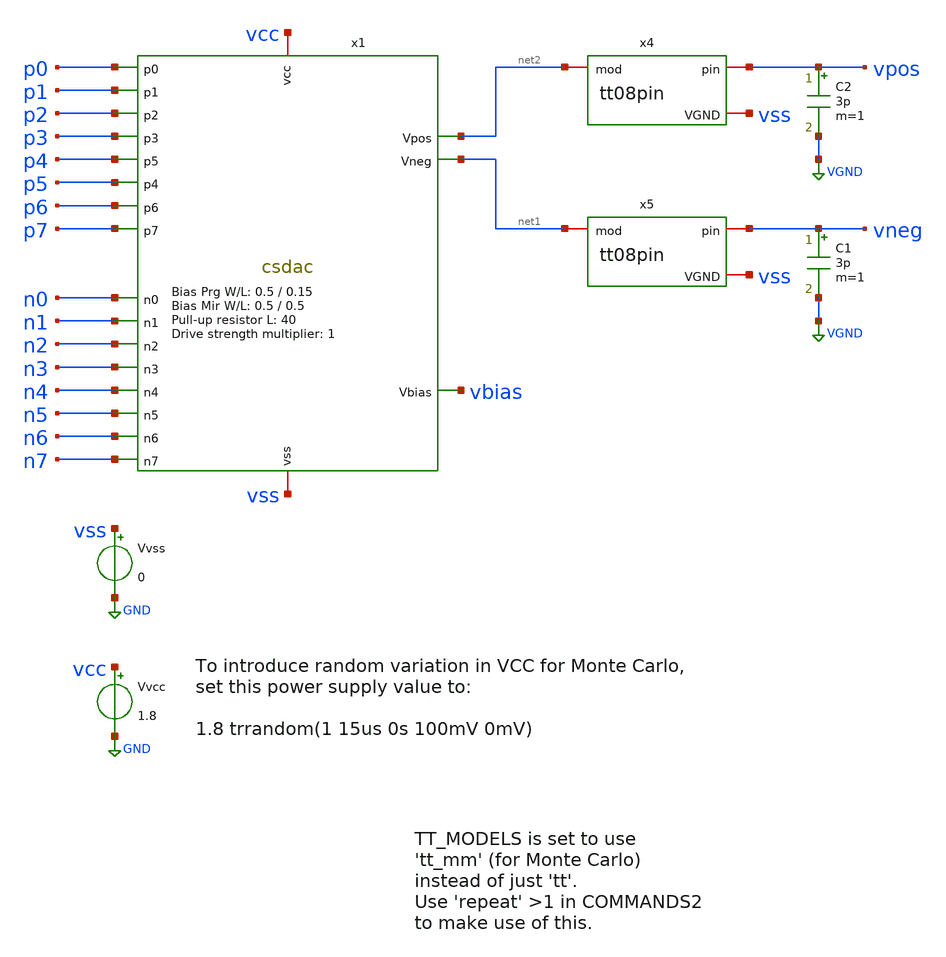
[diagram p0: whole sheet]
** sch_path: xschem/tb_csdac.sch
**.subckt tb_csdac
Vvcc vcc GND 1.8
Vvss vss GND 0
x1 vcc vss p0 p1 p2 p3 p4 p5 p6 p7 n0 n1 n2 n3 n4 n5 n6 n7 net2 net1 vbias csdac RPUL=40 MULTI=1
+ BIASPRG_W=0.5 BIASPRG_L=0.15 BIASMIR_W=0.5 BIASMIR_L=0.5
x4 vpos net2 vss tt08pin
x5 vneg net1 vss tt08pin
C2 vpos VGND 3p m=1
C1 vneg VGND 3p m=1
**** begin user architecture code



.param singlebits=0
.IF (singlebits == 1)
* Mode to just test each binary-weighted level:
Vxp0 p0 GND pulse 0v 1.8v 1u 1n 1n 1u 10u
Vxp1 p1 GND pulse 0v 1.8v 2u 1n 1n 1u 10u
Vxp2 p2 GND pulse 0v 1.8v 3u 1n 1n 1u 10u
Vxp3 p3 GND pulse 0v 1.8v 4u 1n 1n 1u 10u
Vxp4 p4 GND pulse 0v 1.8v 5u 1n 1n 1u 10u
Vxp5 p5 GND pulse 0v 1.8v 6u 1n 1n 1u 10u
Vxp6 p6 GND pulse 0v 1.8v 7u 1n 1n 1u 10u
Vxp7 p7 GND pulse 0v 1.8v 8u 1n 1n 1u 10u
Vxn0 n0 GND pulse 1.8v 0v 1u 1n 1n 1u 10u
Vxn1 n1 GND pulse 1.8v 0v 2u 1n 1n 1u 10u
Vxn2 n2 GND pulse 1.8v 0v 3u 1n 1n 1u 10u
Vxn3 n3 GND pulse 1.8v 0v 4u 1n 1n 1u 10u
Vxn4 n4 GND pulse 1.8v 0v 5u 1n 1n 1u 10u
Vxn5 n5 GND pulse 1.8v 0v 6u 1n 1n 1u 10u
Vxn6 n6 GND pulse 1.8v 0v 7u 1n 1n 1u 10u
Vxn7 n7 GND pulse 1.8v 0v 8u 1n 1n 1u 10u
.ELSEIF (singlebits == 0)
* Mode to test full 0..255 trange:
Vxp0 p0 GND pulse 1.8v 0v 0n 1n 1n 39n 80n
Vxp1 p1 GND pulse 1.8v 0v 0n 1n 1n 79n 160n
Vxp2 p2 GND pulse 1.8v 0v 0n 1n 1n 159n 320n
Vxp3 p3 GND pulse 1.8v 0v 0n 1n 1n 319n 640n
Vxp4 p4 GND pulse 1.8v 0v 0n 1n 1n 639n 1280n
Vxp5 p5 GND pulse 1.8v 0v 0n 1n 1n 1279n 2560n
Vxp6 p6 GND pulse 1.8v 0v 0n 1n 1n 2559n 5120n
Vxp7 p7 GND pulse 1.8v 0v 0n 1n 1n 5119n 10240n
Vxn0 n0 GND pulse 0v 1.8v 0n 1n 1n 39n 80n
Vxn1 n1 GND pulse 0v 1.8v 0n 1n 1n 79n 160n
Vxn2 n2 GND pulse 0v 1.8v 0n 1n 1n 159n 320n
Vxn3 n3 GND pulse 0v 1.8v 0n 1n 1n 319n 640n
Vxn4 n4 GND pulse 0v 1.8v 0n 1n 1n 639n 1280n
Vxn5 n5 GND pulse 0v 1.8v 0n 1n 1n 1279n 2560n
Vxn6 n6 GND pulse 0v 1.8v 0n 1n 1n 2559n 5120n
Vxn7 n7 GND pulse 0v 1.8v 0n 1n 1n 5119n 10240n
.ENDIF

.options savecurrents
.control

  * If using Monte Carlo, change to repeat to (say) 5:
  repeat 1
    save all
    tran 1n 12.8u
    write 11.raw i(vvcc) i(vvss) vpos vneg vbias vcc
    set appendwrite
    reset
  end

*  save all
*  *reset
*  *alterparam MPW=4
*  *alterparam MMW=4
*  tran 1n 12.8u
*  write 11.raw i(vvcc) i(vvss) vpos vneg vbias

*  set appendwrite
*  alterparam MPW=4
*  alterparam MMW=4
*  reset
*  tran 1n 12.8u
*  write 11.raw i(vvcc) i(vvss) vpos vneg vbias

.endc




** opencircuitdesign pdks install
.lib $::SKYWATER_MODELS/sky130.lib.spice tt_mm


**** end user architecture code
**.ends

* expanding   symbol:  csdac.sym # of pins=21
** sym_path: xschem/csdac.sym
** sch_path: xschem/csdac.sch
.subckt csdac vcc vss p0 p1 p2 p3 p4 p5 p6 p7 n0 n1 n2 n3 n4 n5 n6 n7 Vpos Vneg Vbias  MULTI=1
+  RPUL=40  BIASPRG_W=0.5 BIASPRG_L=0.15  BIASMIR_W=0.5 BIASMIR_L=0.5
*.iopin vcc
*.iopin vss
*.ipin p0
*.ipin n0
*.ipin p1
*.ipin n1
*.ipin p2
*.ipin n2
*.ipin p3
*.ipin n3
*.ipin p4
*.ipin n4
*.ipin p5
*.ipin n5
*.ipin p6
*.ipin n6
*.ipin p7
*.ipin n7
*.opin Vpos
*.opin Vneg
*.opin Vbias
XMprog Vbias vss vcc vcc sky130_fd_pr__pfet_01v8 L=BIASPRG_L W=BIASPRG_W nf=1 ad='int((nf+1)/2) * W/nf * 0.29'
+ as='int((nf+2)/2) * W/nf * 0.29' pd='2*int((nf+1)/2) * (W/nf + 0.29)' ps='2*int((nf+2)/2) * (W/nf + 0.29)'
+ nrd='0.29 / W' nrs='0.29 / W' sa=0 sb=0 sd=0 mult=1 m=1
XMmirror Vbias Vbias vss vss sky130_fd_pr__nfet_01v8 L=BIASMIR_L W=BIASMIR_W nf=1 ad='int((nf+1)/2) * W/nf * 0.29'
+ as='int((nf+2)/2) * W/nf * 0.29' pd='2*int((nf+1)/2) * (W/nf + 0.29)' ps='2*int((nf+2)/2) * (W/nf + 0.29)'
+ nrd='0.29 / W' nrs='0.29 / W' sa=0 sb=0 sd=0 mult=1 m=1
XMB0 IS0 Vbias vss vss sky130_fd_pr__nfet_01v8 L=16 W=0.5 nf=1 ad='int((nf+1)/2) * W/nf * 0.29' as='int((nf+2)/2) * W/nf * 0.29'
+ pd='2*int((nf+1)/2) * (W/nf + 0.29)' ps='2*int((nf+2)/2) * (W/nf + 0.29)' nrd='0.29 / W' nrs='0.29 / W'
+ sa=0 sb=0 sd=0 mult=MULTI m=MULTI
XMP0 Vpos p0 IS0 vss sky130_fd_pr__nfet_01v8 L=0.15 W=0.5 nf=1 ad='int((nf+1)/2) * W/nf * 0.29' as='int((nf+2)/2) * W/nf * 0.29'
+ pd='2*int((nf+1)/2) * (W/nf + 0.29)' ps='2*int((nf+2)/2) * (W/nf + 0.29)' nrd='0.29 / W' nrs='0.29 / W'
+ sa=0 sb=0 sd=0 mult=MULTI m=MULTI
XMN0 Vneg n0 IS0 vss sky130_fd_pr__nfet_01v8 L=0.15 W=0.5 nf=1 ad='int((nf+1)/2) * W/nf * 0.29' as='int((nf+2)/2) * W/nf * 0.29'
+ pd='2*int((nf+1)/2) * (W/nf + 0.29)' ps='2*int((nf+2)/2) * (W/nf + 0.29)' nrd='0.29 / W' nrs='0.29 / W'
+ sa=0 sb=0 sd=0 mult=MULTI m=MULTI
XMB1 IS1 Vbias vss vss sky130_fd_pr__nfet_01v8 L=8 W=0.5 nf=1 ad='int((nf+1)/2) * W/nf * 0.29' as='int((nf+2)/2) * W/nf * 0.29'
+ pd='2*int((nf+1)/2) * (W/nf + 0.29)' ps='2*int((nf+2)/2) * (W/nf + 0.29)' nrd='0.29 / W' nrs='0.29 / W'
+ sa=0 sb=0 sd=0 mult=MULTI m=MULTI
XMP1 Vpos p1 IS1 vss sky130_fd_pr__nfet_01v8 L=0.15 W=0.5 nf=1 ad='int((nf+1)/2) * W/nf * 0.29' as='int((nf+2)/2) * W/nf * 0.29'
+ pd='2*int((nf+1)/2) * (W/nf + 0.29)' ps='2*int((nf+2)/2) * (W/nf + 0.29)' nrd='0.29 / W' nrs='0.29 / W'
+ sa=0 sb=0 sd=0 mult=MULTI m=MULTI
XMN1 Vneg n1 IS1 vss sky130_fd_pr__nfet_01v8 L=0.15 W=0.5 nf=1 ad='int((nf+1)/2) * W/nf * 0.29' as='int((nf+2)/2) * W/nf * 0.29'
+ pd='2*int((nf+1)/2) * (W/nf + 0.29)' ps='2*int((nf+2)/2) * (W/nf + 0.29)' nrd='0.29 / W' nrs='0.29 / W'
+ sa=0 sb=0 sd=0 mult=MULTI m=MULTI
XMB2 IS2 Vbias vss vss sky130_fd_pr__nfet_01v8 L=4 W=0.5 nf=1 ad='int((nf+1)/2) * W/nf * 0.29' as='int((nf+2)/2) * W/nf * 0.29'
+ pd='2*int((nf+1)/2) * (W/nf + 0.29)' ps='2*int((nf+2)/2) * (W/nf + 0.29)' nrd='0.29 / W' nrs='0.29 / W'
+ sa=0 sb=0 sd=0 mult=MULTI m=MULTI
XMP2 Vpos p2 IS2 vss sky130_fd_pr__nfet_01v8 L=0.15 W=0.5 nf=1 ad='int((nf+1)/2) * W/nf * 0.29' as='int((nf+2)/2) * W/nf * 0.29'
+ pd='2*int((nf+1)/2) * (W/nf + 0.29)' ps='2*int((nf+2)/2) * (W/nf + 0.29)' nrd='0.29 / W' nrs='0.29 / W'
+ sa=0 sb=0 sd=0 mult=MULTI m=MULTI
XMN2 Vneg n2 IS2 vss sky130_fd_pr__nfet_01v8 L=0.15 W=0.5 nf=1 ad='int((nf+1)/2) * W/nf * 0.29' as='int((nf+2)/2) * W/nf * 0.29'
+ pd='2*int((nf+1)/2) * (W/nf + 0.29)' ps='2*int((nf+2)/2) * (W/nf + 0.29)' nrd='0.29 / W' nrs='0.29 / W'
+ sa=0 sb=0 sd=0 mult=MULTI m=MULTI
XMB3 IS3 Vbias vss vss sky130_fd_pr__nfet_01v8 L=2.1 W=0.5 nf=1 ad='int((nf+1)/2) * W/nf * 0.29' as='int((nf+2)/2) * W/nf * 0.29'
+ pd='2*int((nf+1)/2) * (W/nf + 0.29)' ps='2*int((nf+2)/2) * (W/nf + 0.29)' nrd='0.29 / W' nrs='0.29 / W'
+ sa=0 sb=0 sd=0 mult=MULTI m=MULTI
XMP3 Vpos p3 IS3 vss sky130_fd_pr__nfet_01v8 L=0.15 W=0.5 nf=1 ad='int((nf+1)/2) * W/nf * 0.29' as='int((nf+2)/2) * W/nf * 0.29'
+ pd='2*int((nf+1)/2) * (W/nf + 0.29)' ps='2*int((nf+2)/2) * (W/nf + 0.29)' nrd='0.29 / W' nrs='0.29 / W'
+ sa=0 sb=0 sd=0 mult=MULTI m=MULTI
XMN3 Vneg n3 IS3 vss sky130_fd_pr__nfet_01v8 L=0.15 W=0.5 nf=1 ad='int((nf+1)/2) * W/nf * 0.29' as='int((nf+2)/2) * W/nf * 0.29'
+ pd='2*int((nf+1)/2) * (W/nf + 0.29)' ps='2*int((nf+2)/2) * (W/nf + 0.29)' nrd='0.29 / W' nrs='0.29 / W'
+ sa=0 sb=0 sd=0 mult=MULTI m=MULTI
XMB4 IS4 Vbias vss vss sky130_fd_pr__nfet_01v8 L=1 W=0.5 nf=1 ad='int((nf+1)/2) * W/nf * 0.29' as='int((nf+2)/2) * W/nf * 0.29'
+ pd='2*int((nf+1)/2) * (W/nf + 0.29)' ps='2*int((nf+2)/2) * (W/nf + 0.29)' nrd='0.29 / W' nrs='0.29 / W'
+ sa=0 sb=0 sd=0 mult=MULTI m=MULTI
XMP4 Vpos p4 IS4 vss sky130_fd_pr__nfet_01v8 L=0.15 W=0.5 nf=1 ad='int((nf+1)/2) * W/nf * 0.29' as='int((nf+2)/2) * W/nf * 0.29'
+ pd='2*int((nf+1)/2) * (W/nf + 0.29)' ps='2*int((nf+2)/2) * (W/nf + 0.29)' nrd='0.29 / W' nrs='0.29 / W'
+ sa=0 sb=0 sd=0 mult=MULTI m=MULTI
XMN4 Vneg n4 IS4 vss sky130_fd_pr__nfet_01v8 L=0.15 W=0.5 nf=1 ad='int((nf+1)/2) * W/nf * 0.29' as='int((nf+2)/2) * W/nf * 0.29'
+ pd='2*int((nf+1)/2) * (W/nf + 0.29)' ps='2*int((nf+2)/2) * (W/nf + 0.29)' nrd='0.29 / W' nrs='0.29 / W'
+ sa=0 sb=0 sd=0 mult=MULTI m=MULTI
XMB5 IS5 Vbias vss vss sky130_fd_pr__nfet_01v8 L=2.3 W=1.9 nf=1 ad='int((nf+1)/2) * W/nf * 0.29' as='int((nf+2)/2) * W/nf * 0.29'
+ pd='2*int((nf+1)/2) * (W/nf + 0.29)' ps='2*int((nf+2)/2) * (W/nf + 0.29)' nrd='0.29 / W' nrs='0.29 / W'
+ sa=0 sb=0 sd=0 mult=MULTI m=MULTI
XMP5 Vpos p5 IS5 vss sky130_fd_pr__nfet_01v8 L=0.15 W=1 nf=1 ad='int((nf+1)/2) * W/nf * 0.29' as='int((nf+2)/2) * W/nf * 0.29'
+ pd='2*int((nf+1)/2) * (W/nf + 0.29)' ps='2*int((nf+2)/2) * (W/nf + 0.29)' nrd='0.29 / W' nrs='0.29 / W'
+ sa=0 sb=0 sd=0 mult=MULTI m=MULTI
XMN5 Vneg n5 IS5 vss sky130_fd_pr__nfet_01v8 L=0.15 W=1 nf=1 ad='int((nf+1)/2) * W/nf * 0.29' as='int((nf+2)/2) * W/nf * 0.29'
+ pd='2*int((nf+1)/2) * (W/nf + 0.29)' ps='2*int((nf+2)/2) * (W/nf + 0.29)' nrd='0.29 / W' nrs='0.29 / W'
+ sa=0 sb=0 sd=0 mult=MULTI m=MULTI
XMB6 IS6 Vbias vss vss sky130_fd_pr__nfet_01v8 L=0.5 W=1.1 nf=1 ad='int((nf+1)/2) * W/nf * 0.29' as='int((nf+2)/2) * W/nf * 0.29'
+ pd='2*int((nf+1)/2) * (W/nf + 0.29)' ps='2*int((nf+2)/2) * (W/nf + 0.29)' nrd='0.29 / W' nrs='0.29 / W'
+ sa=0 sb=0 sd=0 mult=MULTI m=MULTI
XMP6 Vpos p6 IS6 vss sky130_fd_pr__nfet_01v8 L=0.15 W=2 nf=1 ad='int((nf+1)/2) * W/nf * 0.29' as='int((nf+2)/2) * W/nf * 0.29'
+ pd='2*int((nf+1)/2) * (W/nf + 0.29)' ps='2*int((nf+2)/2) * (W/nf + 0.29)' nrd='0.29 / W' nrs='0.29 / W'
+ sa=0 sb=0 sd=0 mult=MULTI m=MULTI
XMN6 Vneg n6 IS6 vss sky130_fd_pr__nfet_01v8 L=0.15 W=2 nf=1 ad='int((nf+1)/2) * W/nf * 0.29' as='int((nf+2)/2) * W/nf * 0.29'
+ pd='2*int((nf+1)/2) * (W/nf + 0.29)' ps='2*int((nf+2)/2) * (W/nf + 0.29)' nrd='0.29 / W' nrs='0.29 / W'
+ sa=0 sb=0 sd=0 mult=MULTI m=MULTI
XMB7 IS7 Vbias vss vss sky130_fd_pr__nfet_01v8 L=0.5 W=2.1 nf=1 ad='int((nf+1)/2) * W/nf * 0.29' as='int((nf+2)/2) * W/nf * 0.29'
+ pd='2*int((nf+1)/2) * (W/nf + 0.29)' ps='2*int((nf+2)/2) * (W/nf + 0.29)' nrd='0.29 / W' nrs='0.29 / W'
+ sa=0 sb=0 sd=0 mult=MULTI m=MULTI
XMP7 Vpos p7 IS7 vss sky130_fd_pr__nfet_01v8 L=0.15 W=3 nf=1 ad='int((nf+1)/2) * W/nf * 0.29' as='int((nf+2)/2) * W/nf * 0.29'
+ pd='2*int((nf+1)/2) * (W/nf + 0.29)' ps='2*int((nf+2)/2) * (W/nf + 0.29)' nrd='0.29 / W' nrs='0.29 / W'
+ sa=0 sb=0 sd=0 mult=MULTI m=MULTI
XMN7 Vneg n7 IS7 vss sky130_fd_pr__nfet_01v8 L=0.15 W=3 nf=1 ad='int((nf+1)/2) * W/nf * 0.29' as='int((nf+2)/2) * W/nf * 0.29'
+ pd='2*int((nf+1)/2) * (W/nf + 0.29)' ps='2*int((nf+2)/2) * (W/nf + 0.29)' nrd='0.29 / W' nrs='0.29 / W'
+ sa=0 sb=0 sd=0 mult=MULTI m=MULTI
XR5 Vpos vcc vss sky130_fd_pr__res_high_po_5p73 L=RPUL mult=1 m=1
XR6 Vneg vcc vss sky130_fd_pr__res_high_po_5p73 L=RPUL mult=1 m=1
.ends


* expanding   symbol:  tt08pin.sym # of pins=3
** sym_path: xschem/tt08pin.sym
** sch_path: xschem/tt08pin.sch
.subckt tt08pin pin mod VGND
*.iopin pin
*.iopin VGND
*.iopin mod
R1 net1 pin 1 m=1
C1 pin VGND 1p m=1
L1 net2 net1 1n m=1
V1 VAPWR VGND 3.3
C2 net2 VGND 2p m=1
R2 net3 net2 50 m=1
XM2 net3 VGND mod VAPWR sky130_fd_pr__pfet_g5v0d10v5 L=0.5 W=100 nf=20 ad='int((nf+1)/2) * W/nf * 0.29'
+ as='int((nf+2)/2) * W/nf * 0.29' pd='2*int((nf+1)/2) * (W/nf + 0.29)' ps='2*int((nf+2)/2) * (W/nf + 0.29)'
+ nrd='0.29 / W' nrs='0.29 / W' sa=0 sb=0 sd=0 mult=1 m=1
XM1 net3 VAPWR mod VGND sky130_fd_pr__nfet_g5v0d10v5 L=0.5 W=60 nf=12 ad='int((nf+1)/2) * W/nf * 0.29'
+ as='int((nf+2)/2) * W/nf * 0.29' pd='2*int((nf+1)/2) * (W/nf + 0.29)' ps='2*int((nf+2)/2) * (W/nf + 0.29)'
+ nrd='0.29 / W' nrs='0.29 / W' sa=0 sb=0 sd=0 mult=1 m=1
XM4 net3 VAPWR VGND VAPWR sky130_fd_pr__pfet_g5v0d10v5 L=0.5 W=100 nf=20 ad='int((nf+1)/2) * W/nf * 0.29'
+ as='int((nf+2)/2) * W/nf * 0.29' pd='2*int((nf+1)/2) * (W/nf + 0.29)' ps='2*int((nf+2)/2) * (W/nf + 0.29)'
+ nrd='0.29 / W' nrs='0.29 / W' sa=0 sb=0 sd=0 mult=15 m=15
XM3 net3 VGND VGND VGND sky130_fd_pr__nfet_g5v0d10v5 L=0.5 W=60 nf=12 ad='int((nf+1)/2) * W/nf * 0.29'
+ as='int((nf+2)/2) * W/nf * 0.29' pd='2*int((nf+1)/2) * (W/nf + 0.29)' ps='2*int((nf+2)/2) * (W/nf + 0.29)'
+ nrd='0.29 / W' nrs='0.29 / W' sa=0 sb=0 sd=0 mult=15 m=15
C3 mod VGND 250f m=1
.ends

.GLOBAL GND
.GLOBAL VGND
.GLOBAL VAPWR
.end
